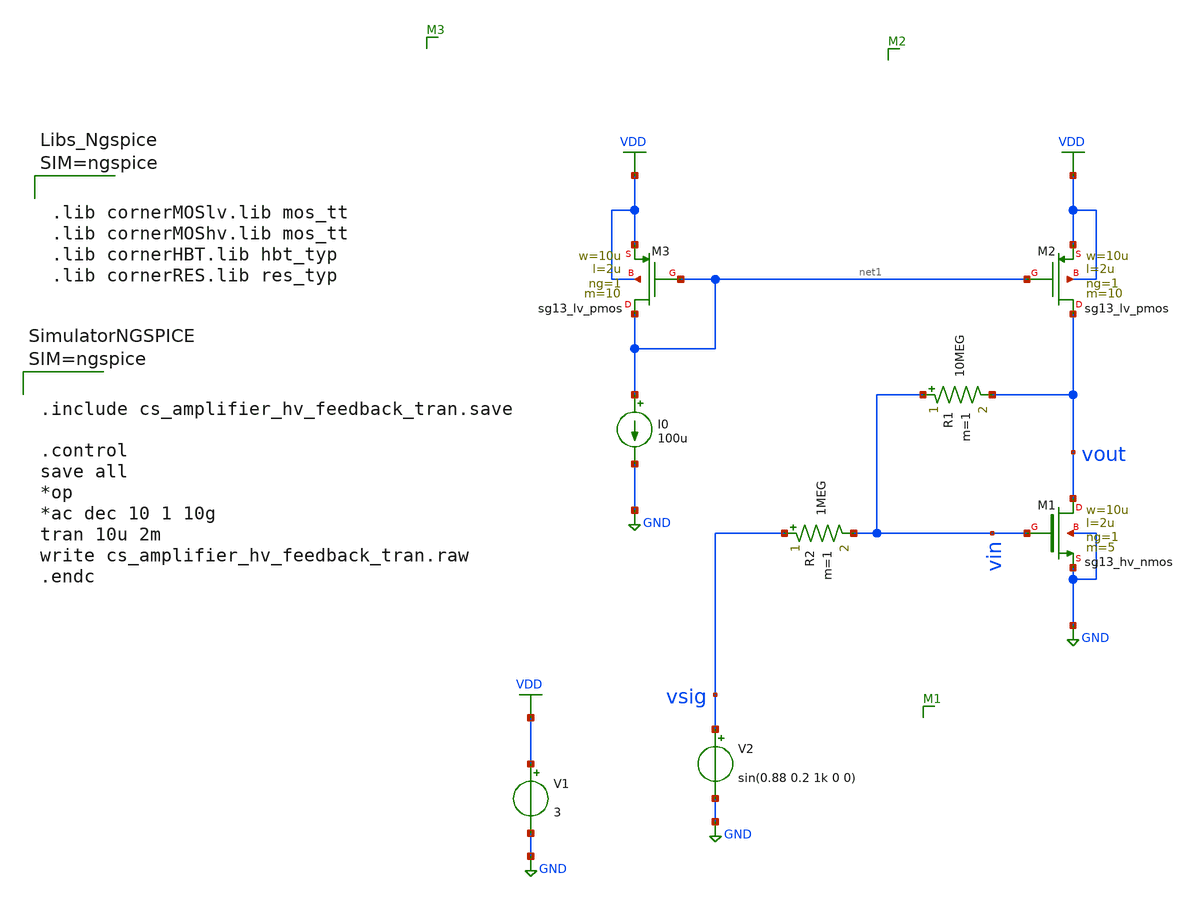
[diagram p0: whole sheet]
** sch_path: Schematics/lab_1/cs_amplifier_hv_feedback_tran.sch
**.subckt cs_amplifier_hv_feedback_tran
V1 VDD GND 3
V2 vsig GND sin(0.88 0.2 1k 0 0)
XM1 vout vin GND GND sg13_hv_nmos w=10u l=2u ng=1 m=5 mm_ok=1
R2 vsig vin 1MEG m=1
XM2 vout net1 VDD VDD sg13_lv_pmos w=10u l=2u ng=1 m=10 mm_ok=1
I0 net1 GND 100u
R1 vin vout 10MEG m=1
XM3 net1 net1 VDD VDD sg13_lv_pmos w=10u l=2u ng=1 m=10 mm_ok=1
**** begin user architecture code



.lib cornerMOSlv.lib mos_tt
.lib cornerMOShv.lib mos_tt
.lib cornerHBT.lib hbt_typ
.lib cornerRES.lib res_typ






.include cs_amplifier_hv_feedback_tran.save

.control
save all
*op
*ac dec 10 1 10g
tran 10u 2m
write cs_amplifier_hv_feedback_tran.raw
.endc



**** end user architecture code
**.ends
.GLOBAL GND
.GLOBAL VDD
.end
